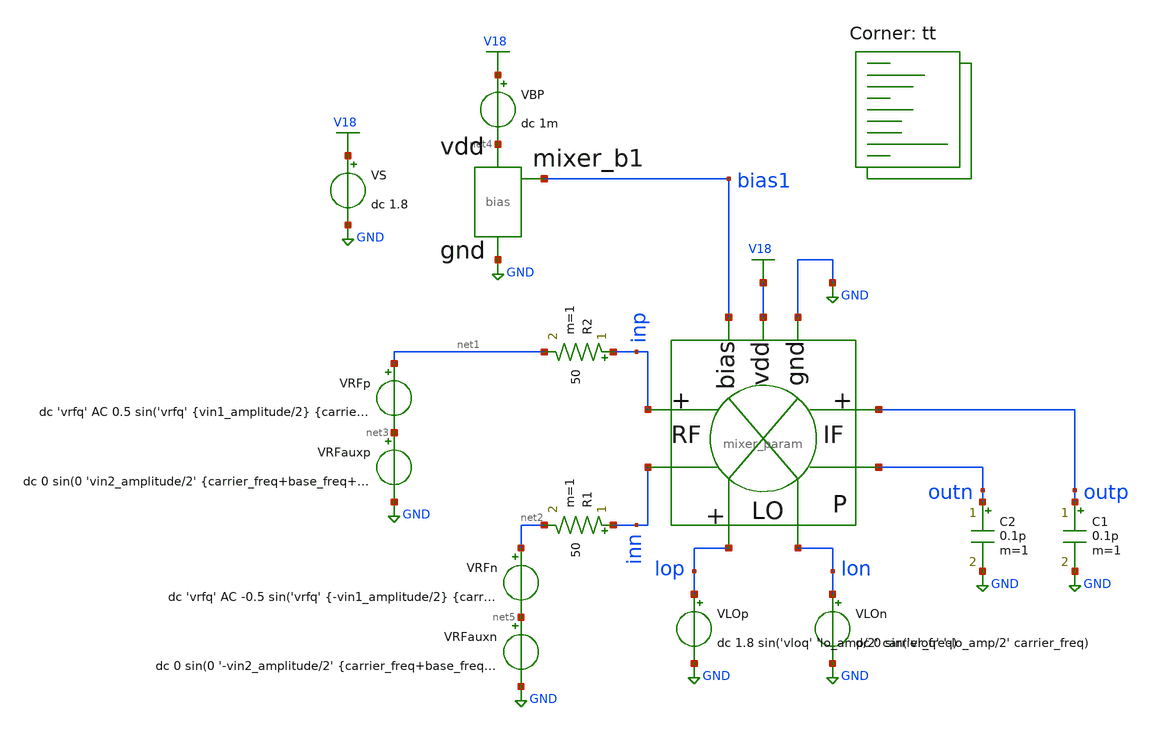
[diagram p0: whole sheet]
** sch_path: xschem/mixer_transfer_tb.sch
**.subckt mixer_transfer_tb
VRFp net1 net3 dc 'vrfq' AC 0.5 sin('vrfq' {vin1_amplitude/2} {carrier_freq+base_freq})
VLOp lop GND dc 1.8 sin('vloq' 'lo_amp/2' carrier_freq)
R2 inp net1 50 m=1
VLOn lon GND dc 0 sin('vloq' '-lo_amp/2' carrier_freq)
VS V18 GND dc 1.8
VBP V18 net4 dc 1m
C1 outp GND 0.1p m=1
C2 outn GND 0.1p m=1
VRFauxp net3 GND dc 0 sin(0 'vin2_amplitude/2' {carrier_freq+base_freq+delta_freq})
X2 inp inn outp outn lon lop bias1 V18 GND mixer_param
VRFn net2 net5 dc 'vrfq' AC -0.5 sin('vrfq' {-vin1_amplitude/2} {carrier_freq+base_freq})
VRFauxn net5 GND dc 0 sin(0 '-vin2_amplitude/2' {carrier_freq+base_freq+delta_freq})
R1 inn net2 50 m=1
X1 bias1 net4 GND bias
**** begin user architecture code
.lib $::SKYWATER_MODELS/sky130.lib.spice tt


*.control
*tran 10p 5us
*save all
*write tb_gain.raw
*.endc




.option TRTOL=5
.option SCALE=1e-6

.param carrier_freq=900Meg
.param base_freq=5Meg
.param delta_freq=1Meg
.param vin1_amplitude=10e-3
.param vin2_amplitude=10e-3
.param vrfq=1.2
.param vloq=0.8
.param lo_amp=1.2

.param bias_width=0.75
.param mixer_biasfactor=5
.param mixer_m23width=10
.param mixer_m23fingers=4
.param mixer_m4567width=2
.param mixer_m4567fingers=1
.param mixer_rw=2.85
.param mixer_rl=22.8


**** end user architecture code
**.ends

* expanding   symbol:  opensubghz/xschem/mixer_param.sym # of pins=9
** sym_path: xschem/mixer_param.sym
** sch_path: xschem/mixer_param.sch
.subckt mixer_param RFp RFn IFp IFn LOn LOp bias vdd gnd
*.ipin LOp
*.ipin RFp
*.ipin RFn
*.ipin LOn
*.ipin bias
*.iopin gnd
*.iopin vdd
*.opin IFp
*.opin IFn
XM2 net1 RFp cm1 GND sky130_fd_pr__nfet_01v8 L=0.15 W='mixer_m23width' nf='mixer_m23fingers' ad='int((nf+1)/2) * W/nf * 0.29'
+ as='int((nf+2)/2) * W/nf * 0.29' pd='2*int((nf+1)/2) * (W/nf + 0.29)' ps='2*int((nf+2)/2) * (W/nf + 0.29)'
+ nrd='0.29 / W' nrs='0.29 / W' sa=0 sb=0 sd=0 mult=1 m=1
XM1 net2 bias gnd GND sky130_fd_pr__nfet_01v8 L=0.15 W='bias_width*mixer_biasfactor' nf='mixer_biasfactor'
+ ad='int((nf+1)/2) * W/nf * 0.29' as='int((nf+2)/2) * W/nf * 0.29' pd='2*int((nf+1)/2) * (W/nf + 0.29)'
+ ps='2*int((nf+2)/2) * (W/nf + 0.29)' nrd='0.29 / W' nrs='0.29 / W' sa=0 sb=0 sd=0 mult=1 m=1
XM3 net3 RFn cm1 GND sky130_fd_pr__nfet_01v8 L=0.15 W='mixer_m23width' nf='mixer_m23fingers' ad='int((nf+1)/2) * W/nf * 0.29'
+ as='int((nf+2)/2) * W/nf * 0.29' pd='2*int((nf+1)/2) * (W/nf + 0.29)' ps='2*int((nf+2)/2) * (W/nf + 0.29)'
+ nrd='0.29 / W' nrs='0.29 / W' sa=0 sb=0 sd=0 mult=1 m=1
XM4 IFp LOp cm2a GND sky130_fd_pr__nfet_01v8 L=0.15 W='mixer_m4567width' nf='mixer_m4567fingers' ad='int((nf+1)/2) * W/nf * 0.29'
+ as='int((nf+2)/2) * W/nf * 0.29' pd='2*int((nf+1)/2) * (W/nf + 0.29)' ps='2*int((nf+2)/2) * (W/nf + 0.29)'
+ nrd='0.29 / W' nrs='0.29 / W' sa=0 sb=0 sd=0 mult=1 m=1
XM5 IFn LOn cm2a GND sky130_fd_pr__nfet_01v8 L=0.15 W='mixer_m4567width' nf='mixer_m4567fingers' ad='int((nf+1)/2) * W/nf * 0.29'
+ as='int((nf+2)/2) * W/nf * 0.29' pd='2*int((nf+1)/2) * (W/nf + 0.29)' ps='2*int((nf+2)/2) * (W/nf + 0.29)'
+ nrd='0.29 / W' nrs='0.29 / W' sa=0 sb=0 sd=0 mult=1 m=1
XM6 IFp LOn cm2b GND sky130_fd_pr__nfet_01v8 L=0.15 W='mixer_m4567width' nf='mixer_m4567fingers' ad='int((nf+1)/2) * W/nf * 0.29'
+ as='int((nf+2)/2) * W/nf * 0.29' pd='2*int((nf+1)/2) * (W/nf + 0.29)' ps='2*int((nf+2)/2) * (W/nf + 0.29)'
+ nrd='0.29 / W' nrs='0.29 / W' sa=0 sb=0 sd=0 mult=1 m=1
XM7 IFn LOp cm2b GND sky130_fd_pr__nfet_01v8 L=0.15 W='mixer_m4567width' nf='mixer_m4567fingers' ad='int((nf+1)/2) * W/nf * 0.29'
+ as='int((nf+2)/2) * W/nf * 0.29' pd='2*int((nf+1)/2) * (W/nf + 0.29)' ps='2*int((nf+2)/2) * (W/nf + 0.29)'
+ nrd='0.29 / W' nrs='0.29 / W' sa=0 sb=0 sd=0 mult=1 m=1
Vscm1 cm1 net2 dc 0
Vscm2b cm2b net3 dc 0
Vscm2a cm2a net1 dc 0
XR1 IFp vdd gnd sky130_fd_pr__res_xhigh_po_5p73 L='mixer_rl' mult=1 m=1
XR2 IFn vdd gnd sky130_fd_pr__res_xhigh_po_5p73 L='mixer_rl' mult=1 m=1
.ends


* expanding   symbol:  opensubghz/xschem/bias.sym # of pins=3
** sym_path: xschem/bias.sym
** sch_path: xschem/bias.sch
.subckt bias mixer_b1 vdd gnd
*.iopin vdd
*.opin mixer_b1
*.iopin gnd
XM1 net1 mixer_b1 gnd GND sky130_fd_pr__nfet_01v8 L=0.15 W=bias_width nf=1 ad='int((nf+1)/2) * W/nf * 0.29'
+ as='int((nf+2)/2) * W/nf * 0.29' pd='2*int((nf+1)/2) * (W/nf + 0.29)' ps='2*int((nf+2)/2) * (W/nf + 0.29)'
+ nrd='0.29 / W' nrs='0.29 / W' sa=0 sb=0 sd=0 mult=1 m=1
XR1 mixer_b1 vdd gnd sky130_fd_pr__res_xhigh_po_0p35 L=1.5 mult=1 m=1
Vsense mixer_b1 net1 0
.ends

.GLOBAL V18
.GLOBAL GND
.end
